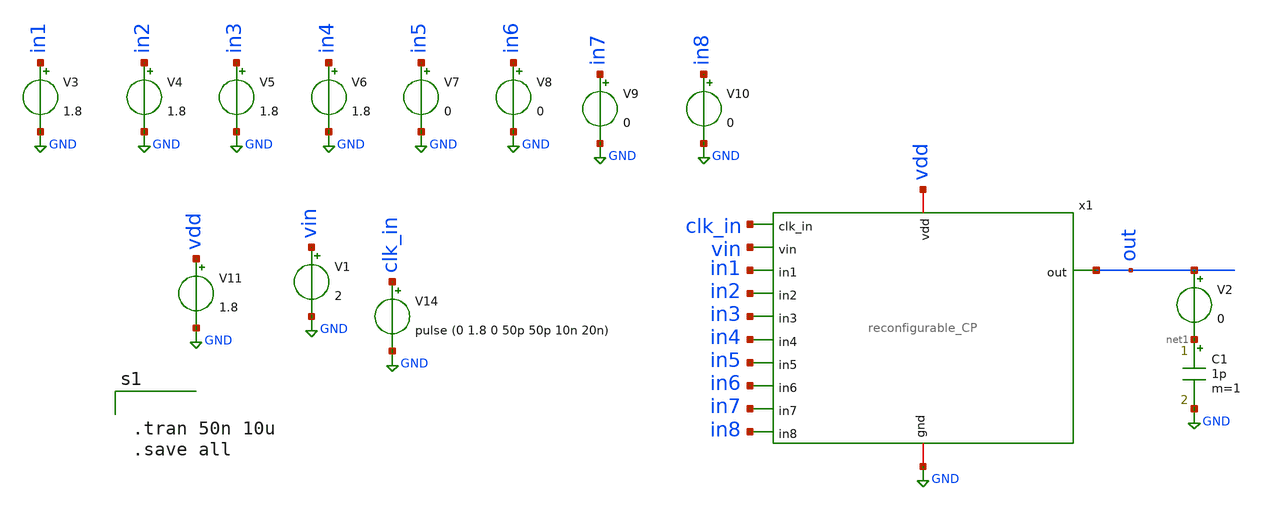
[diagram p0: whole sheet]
** sch_path: xschem/charge_pumps2/CP_withCMFB.sch
**.subckt CP_withCMFB
x1 clk_in vin out in1 in2 in3 in4 in5 in6 in7 in8 vdd GND reconfigurable_CP
V3 in1 GND 1.8
V4 in2 GND 1.8
V5 in3 GND 1.8
V6 in4 GND 1.8
V7 in5 GND 0
V8 in6 GND 0
V9 in7 GND 0
V10 in8 GND 0
V1 vin GND 2
V11 vdd GND 1.8
V14 clk_in GND pulse (0 1.8 0 50p 50p 10n 20n)
C1 net1 GND 1p m=1
V2 out net1 0
**** begin user architecture code


.tran 50n 10u
.save all



** opencircuitdesign pdks install
.lib $::SKYWATER_MODELS/sky130.lib.spice tt


**** end user architecture code
**.ends
.GLOBAL GND
.end
